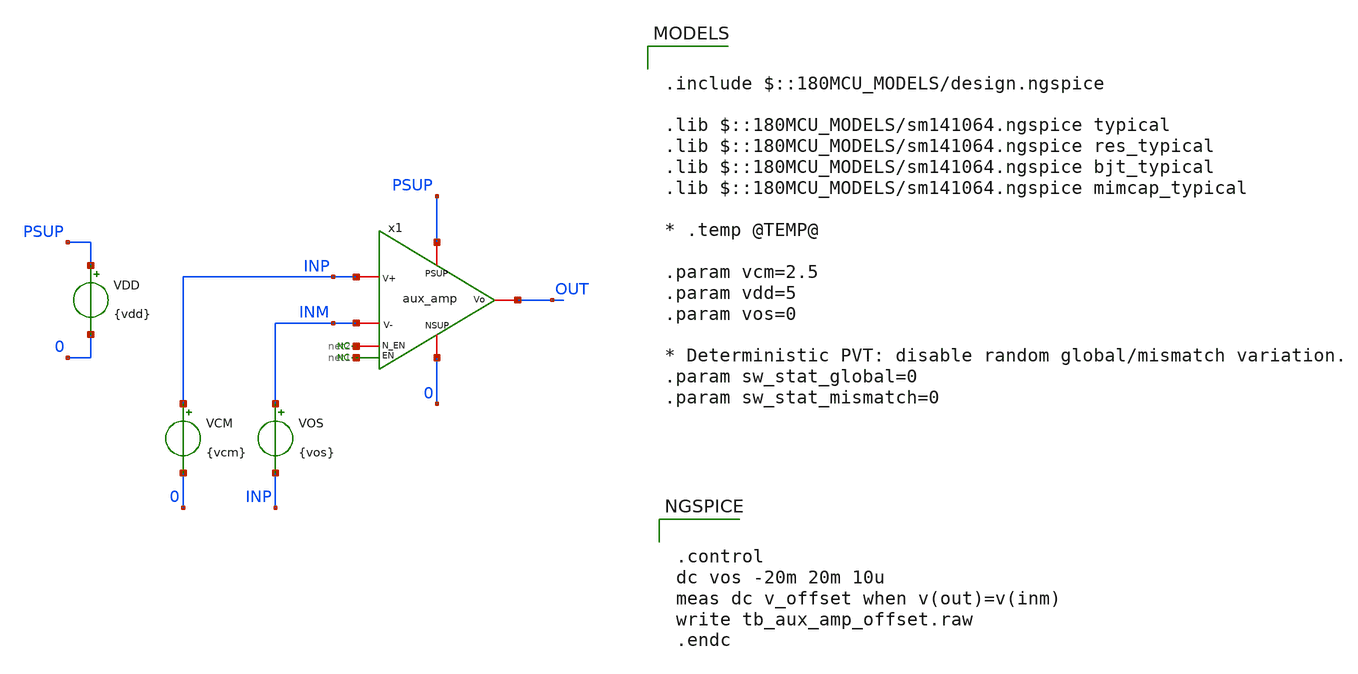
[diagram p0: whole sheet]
** sch_path: xschem/blocks/error_amp/tb_aux_amp_offset.sch
**.subckt tb_aux_amp_offset
VDD PSUP 0 {vdd}
VCM INP 0 {vcm}
* noconn #net1
* noconn #net2
x1 PSUP OUT INP INM net2 0 net1 aux_amp
VOS INM INP {vos}
**** begin user architecture code


.control
dc vos -20m 20m 10u
meas dc v_offset when v(out)=v(inm)
write tb_aux_amp_offset.raw
.endc



.include $::180MCU_MODELS/design.ngspice

.lib $::180MCU_MODELS/sm141064.ngspice typical
.lib $::180MCU_MODELS/sm141064.ngspice res_typical
.lib $::180MCU_MODELS/sm141064.ngspice bjt_typical
.lib $::180MCU_MODELS/sm141064.ngspice mimcap_typical

* .temp @TEMP@

.param vcm=2.5
.param vdd=5
.param vos=0

* Deterministic PVT: disable random global/mismatch variation.
.param sw_stat_global=0
.param sw_stat_mismatch=0


**** end user architecture code
**.ends

* expanding   symbol:  blocks/aux_amp/aux_amp.sym # of pins=7
** sym_path: xschem/lib/aux_amp.sym
** sch_path: xschem/lib/aux_amp.sch
.subckt aux_amp PSUP Vo V+ V- N_EN NSUP EN
*.ipin PSUP
*.ipin NSUP
*.ipin N_EN
*.ipin EN
*.ipin V+
*.ipin V-
*.opin Vo
XM1 Vo V- net2 net2 nfet_06v0 L=1.80u W=0.80u nf=1 ad='int((nf+1)/2) * W/nf * 0.18u' as='int((nf+2)/2) * W/nf * 0.18u'
+ pd='2*int((nf+1)/2) * (W/nf + 0.18u)' ps='2*int((nf+2)/2) * (W/nf + 0.18u)' nrd='0.18u / W' nrs='0.18u / W'
+ sa=0 sb=0 sd=0 m=1
XM2 net1 V+ net2 net2 nfet_06v0 L=1.80u W=0.80u nf=1 ad='int((nf+1)/2) * W/nf * 0.18u' as='int((nf+2)/2) * W/nf * 0.18u'
+ pd='2*int((nf+1)/2) * (W/nf + 0.18u)' ps='2*int((nf+2)/2) * (W/nf + 0.18u)' nrd='0.18u / W' nrs='0.18u / W'
+ sa=0 sb=0 sd=0 m=1
XM5 net1 net1 PSUP PSUP pfet_06v0 L=0.55u W=0.30u nf=1 ad='int((nf+1)/2) * W/nf * 0.18u' as='int((nf+2)/2) * W/nf * 0.18u'
+ pd='2*int((nf+1)/2) * (W/nf + 0.18u)' ps='2*int((nf+2)/2) * (W/nf + 0.18u)' nrd='0.18u / W' nrs='0.18u / W'
+ sa=0 sb=0 sd=0 m=1
XM6 Vo net1 PSUP PSUP pfet_06v0 L=0.55u W=0.30u nf=1 ad='int((nf+1)/2) * W/nf * 0.18u' as='int((nf+2)/2) * W/nf * 0.18u'
+ pd='2*int((nf+1)/2) * (W/nf + 0.18u)' ps='2*int((nf+2)/2) * (W/nf + 0.18u)' nrd='0.18u / W' nrs='0.18u / W'
+ sa=0 sb=0 sd=0 m=1
I0 net2 NSUP 5u
* noconn N_EN
* noconn EN
.ends

.end
